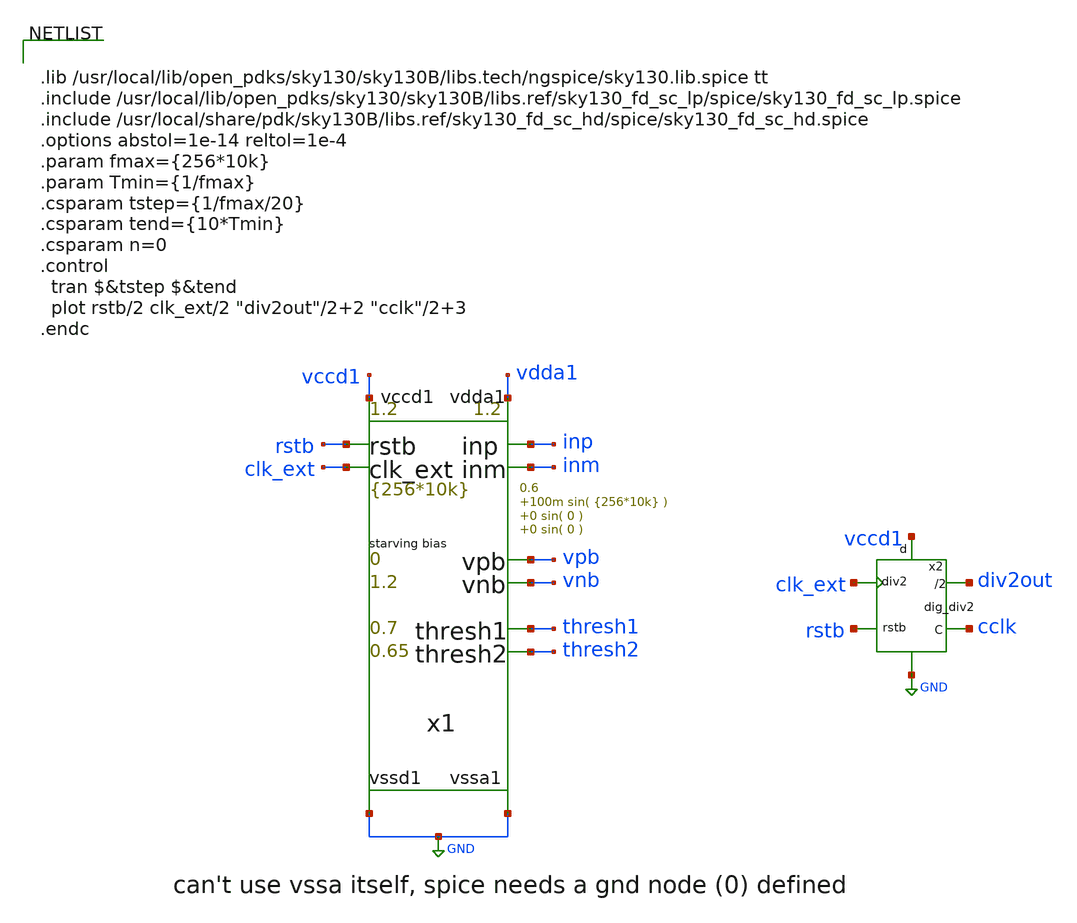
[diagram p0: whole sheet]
** sch_path: xschem/test_bench/dig_div2_tb.sch
**.subckt dig_div2_tb
x1 thresh1 thresh2 vdda1 GND inp inm clk_ext rstb vccd1 GND vpb vnb pad_frame p_vdda1=1.2 p_vccd1=1.2
+ p_fclk={256*10k} p_duty_cycle=0.5 p_rstb_delay={1.5/p_fclk} p_rstb_tr=5n p_thresh1=0.7 p_thresh2=0.65
+ p_vpb=0 p_vnb=1.2 p_vcm=0.6 p_amp1=100m p_f1={256*10k} p_amp2=0 p_f2=0 p_amp3=0 p_f3=0
x2 rstb cclk div2out vccd1 GND clk_ext dig_div2
**** begin user architecture code


.lib /usr/local/lib/open_pdks/sky130/sky130B/libs.tech/ngspice/sky130.lib.spice tt
.include /usr/local/lib/open_pdks/sky130/sky130B/libs.ref/sky130_fd_sc_lp/spice/sky130_fd_sc_lp.spice
.include /usr/local/share/pdk/sky130B/libs.ref/sky130_fd_sc_hd/spice/sky130_fd_sc_hd.spice
.options abstol=1e-14 reltol=1e-4
.param fmax={256*10k}
.param Tmin={1/fmax}
.csparam tstep={1/fmax/20}
.csparam tend={10*Tmin}
.csparam n=0
.control
  tran $&tstep $&tend
  plot rstb/2 clk_ext/2 "div2out"/2+2 "cclk"/2+3
.endc


**** end user architecture code
**.ends

* expanding   symbol:  test_bench/pad_frame.sym # of pins=12
** sym_path: xschem/test_bench/pad_frame.sym
** sch_path: xschem/test_bench/pad_frame.sch
.subckt pad_frame thresh1 thresh2 vdda1 vssa1 inp inm clk_ext rstb vccd1 vssd1 vpb vnb   p_vdda1=1.2
+  p_vccd1=1.2  p_fclk={256*10k}  p_duty_cycle=0.5  p_rstb_delay={1.5/p_fclk}  p_rstb_tr=5n  p_thresh1=0.7
+  p_thresh2=0.65  p_vpb=0  p_vnb=1.2  p_vcm=0.6  p_amp1=100m  p_f1={256*10k}  p_amp2=0  p_f2=0  p_amp3=0
+  p_f3=0
*.opin thresh1
*.opin thresh2
*.opin vdda1
*.opin vssa1
*.opin inp
*.opin inm
*.opin vccd1
*.opin vssd1
*.opin rstb
*.opin clk_ext
*.opin vpb
*.opin vnb
vdda1 vdda1 vssa1 DC {p_vdda1}
vthresh1 thresh1 vssa1 DC {p_thresh1}
vthresh2 thresh2 vssa1 DC {p_thresh2}
vinp1 inp inp2 DC 0 SIN(0 {p_amp1} {p_f1})
vinm1 inm inm2 DC 0 SIN(0 {-p_amp1} {p_f1})
vpb vpb vssa1 DC {p_vpb}
vnb vnb vssa1 DC {p_vnb}
vinp2 inp2 inp3 DC 0 SIN(0 {p_amp2} {p_f2})
vinp3 inp3 vcm DC 0 SIN(0 {p_amp3} {p_f3})
vinm2 inm2 inm3 DC 0 SIN(0 {-p_amp2} {p_f2})
vinm3 inm3 vcm DC 0 SIN(0 {-p_amp3} {p_f3})
vcm vcm vssa1 DC {p_vcm}
vdda2 vccd1 vssd1 DC {p_vccd1}
Vclk clk vssd1 DC 0 PULSE (0 p_vccd1 1n 1n 1n {p_duty_cycle*1/p_fclk} {1/p_fclk} 0
Vrstb rstb vssd1 DC 0 PWL ( 0 0 p_rstb_delay 0 {p_rstb_delay + p_rstb_tr} p_vccd1)
x1 clk rstb vssd1 vssd1 vccd1 vccd1 clk_ext sky130_fd_sc_hd__dlclkp_1
.ends


* expanding   symbol:  clkgen/dig_div2.sym # of pins=6
** sym_path: xschem/clkgen/dig_div2.sym
** sch_path: xschem/clkgen/dig_div2.sch
.subckt dig_div2 rstb cclk div2out vccd vssd div2
*.ipin div2
*.ipin rstb
*.opin cclk
*.opin div2out
*.ipin vccd
*.ipin vssd
x11 net3 net1 rstb vssd vssd vccd vccd div2out net1 sky130_fd_sc_hd__dfrbp_1
x2 net2 div2out vssd vssd vccd vccd cclk sky130_fd_sc_hd__and2_0
x1 div2 vssd vssd vccd vccd net4 sky130_fd_sc_hd__buf_1
x3 net4 vssd vssd vccd vccd net5 sky130_fd_sc_hd__buf_1
x4 net5 vssd vssd vccd vccd net2 sky130_fd_sc_hd__buf_1
x5 div2 vssd vssd vccd vccd net3 sky130_fd_sc_hd__inv_1
.ends

.GLOBAL GND
.end
